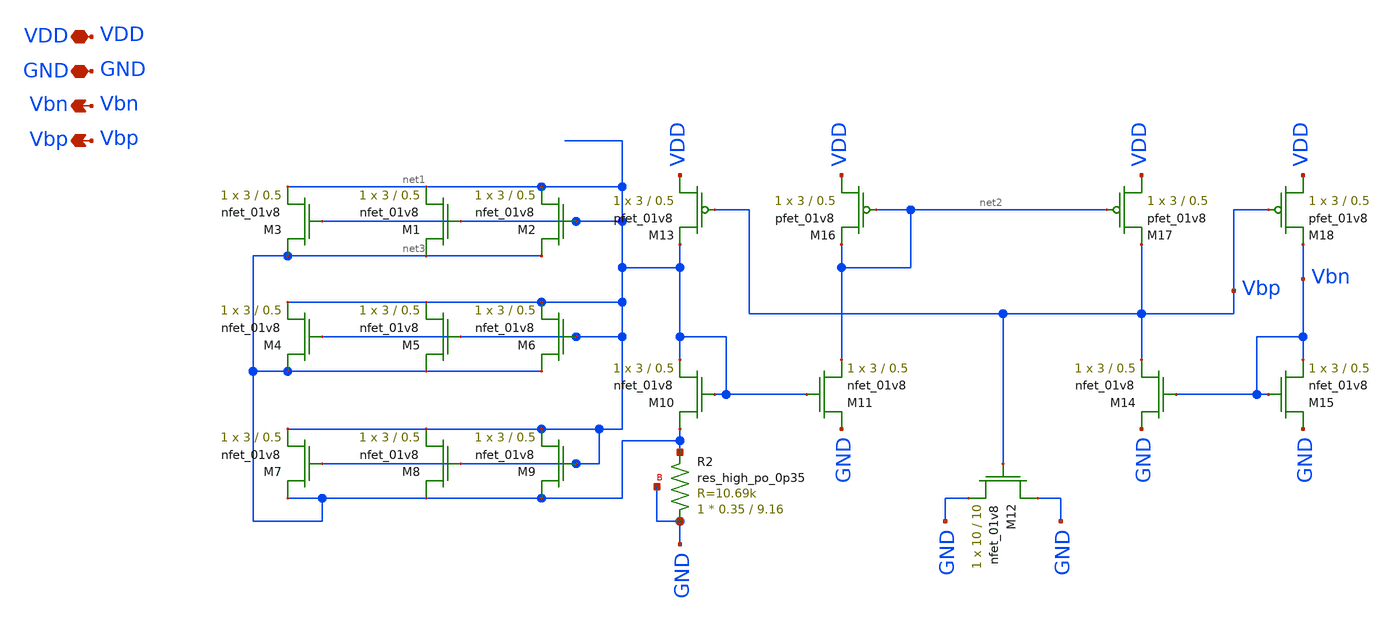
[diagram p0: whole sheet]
** sch_path: final/LDS/bias_gen_LDS.sch
**.subckt bias_gen_LDS VDD Vbp GND Vbn
*.iopin VDD
*.opin Vbp
*.iopin GND
*.opin Vbn
XM12 GND Vbp GND GND sky130_fd_pr__nfet_01v8 L=10 W=10 nf=1 ad='int((nf+1)/2) * W/nf * 0.29' as='int((nf+2)/2) * W/nf * 0.29'
+ pd='2*int((nf+1)/2) * (W/nf + 0.29)' ps='2*int((nf+2)/2) * (W/nf + 0.29)' nrd='0.29 / W' nrs='0.29 / W'
+ sa=0 sb=0 sd=0 mult=1 m=1
XM13 VDD Vbp net1 VDD sky130_fd_pr__pfet_01v8 L=0.5 W=3 nf=1 ad='int((nf+1)/2) * W/nf * 0.29' as='int((nf+2)/2) * W/nf * 0.29'
+ pd='2*int((nf+1)/2) * (W/nf + 0.29)' ps='2*int((nf+2)/2) * (W/nf + 0.29)' nrd='0.29 / W' nrs='0.29 / W'
+ sa=0 sb=0 sd=0 mult=1 m=1
XR2 GND net3 GND sky130_fd_pr__res_high_po_0p35 L=9.16 mult=1 m=1
XM3 net3 net1 net1 GND sky130_fd_pr__nfet_01v8 L=0.5 W=3 nf=1 ad='int((nf+1)/2) * W/nf * 0.29' as='int((nf+2)/2) * W/nf * 0.29'
+ pd='2*int((nf+1)/2) * (W/nf + 0.29)' ps='2*int((nf+2)/2) * (W/nf + 0.29)' nrd='0.29 / W' nrs='0.29 / W'
+ sa=0 sb=0 sd=0 mult=1 m=1
XM1 net3 net1 net1 GND sky130_fd_pr__nfet_01v8 L=0.5 W=3 nf=1 ad='int((nf+1)/2) * W/nf * 0.29' as='int((nf+2)/2) * W/nf * 0.29'
+ pd='2*int((nf+1)/2) * (W/nf + 0.29)' ps='2*int((nf+2)/2) * (W/nf + 0.29)' nrd='0.29 / W' nrs='0.29 / W'
+ sa=0 sb=0 sd=0 mult=1 m=1
XM2 net3 net1 net1 GND sky130_fd_pr__nfet_01v8 L=0.5 W=3 nf=1 ad='int((nf+1)/2) * W/nf * 0.29' as='int((nf+2)/2) * W/nf * 0.29'
+ pd='2*int((nf+1)/2) * (W/nf + 0.29)' ps='2*int((nf+2)/2) * (W/nf + 0.29)' nrd='0.29 / W' nrs='0.29 / W'
+ sa=0 sb=0 sd=0 mult=1 m=1
XM4 net3 net1 net1 GND sky130_fd_pr__nfet_01v8 L=0.5 W=3 nf=1 ad='int((nf+1)/2) * W/nf * 0.29' as='int((nf+2)/2) * W/nf * 0.29'
+ pd='2*int((nf+1)/2) * (W/nf + 0.29)' ps='2*int((nf+2)/2) * (W/nf + 0.29)' nrd='0.29 / W' nrs='0.29 / W'
+ sa=0 sb=0 sd=0 mult=1 m=1
XM5 net3 net1 net1 GND sky130_fd_pr__nfet_01v8 L=0.5 W=3 nf=1 ad='int((nf+1)/2) * W/nf * 0.29' as='int((nf+2)/2) * W/nf * 0.29'
+ pd='2*int((nf+1)/2) * (W/nf + 0.29)' ps='2*int((nf+2)/2) * (W/nf + 0.29)' nrd='0.29 / W' nrs='0.29 / W'
+ sa=0 sb=0 sd=0 mult=1 m=1
XM6 net3 net1 net1 GND sky130_fd_pr__nfet_01v8 L=0.5 W=3 nf=1 ad='int((nf+1)/2) * W/nf * 0.29' as='int((nf+2)/2) * W/nf * 0.29'
+ pd='2*int((nf+1)/2) * (W/nf + 0.29)' ps='2*int((nf+2)/2) * (W/nf + 0.29)' nrd='0.29 / W' nrs='0.29 / W'
+ sa=0 sb=0 sd=0 mult=1 m=1
XM7 net3 net1 net1 GND sky130_fd_pr__nfet_01v8 L=0.5 W=3 nf=1 ad='int((nf+1)/2) * W/nf * 0.29' as='int((nf+2)/2) * W/nf * 0.29'
+ pd='2*int((nf+1)/2) * (W/nf + 0.29)' ps='2*int((nf+2)/2) * (W/nf + 0.29)' nrd='0.29 / W' nrs='0.29 / W'
+ sa=0 sb=0 sd=0 mult=1 m=1
XM8 net3 net1 net1 GND sky130_fd_pr__nfet_01v8 L=0.5 W=3 nf=1 ad='int((nf+1)/2) * W/nf * 0.29' as='int((nf+2)/2) * W/nf * 0.29'
+ pd='2*int((nf+1)/2) * (W/nf + 0.29)' ps='2*int((nf+2)/2) * (W/nf + 0.29)' nrd='0.29 / W' nrs='0.29 / W'
+ sa=0 sb=0 sd=0 mult=1 m=1
XM9 net3 net1 net1 GND sky130_fd_pr__nfet_01v8 L=0.5 W=3 nf=1 ad='int((nf+1)/2) * W/nf * 0.29' as='int((nf+2)/2) * W/nf * 0.29'
+ pd='2*int((nf+1)/2) * (W/nf + 0.29)' ps='2*int((nf+2)/2) * (W/nf + 0.29)' nrd='0.29 / W' nrs='0.29 / W'
+ sa=0 sb=0 sd=0 mult=1 m=1
XM10 net3 net1 net1 GND sky130_fd_pr__nfet_01v8 L=0.5 W=3 nf=1 ad='int((nf+1)/2) * W/nf * 0.29' as='int((nf+2)/2) * W/nf * 0.29'
+ pd='2*int((nf+1)/2) * (W/nf + 0.29)' ps='2*int((nf+2)/2) * (W/nf + 0.29)' nrd='0.29 / W' nrs='0.29 / W'
+ sa=0 sb=0 sd=0 mult=1 m=1
XM11 GND net1 net2 GND sky130_fd_pr__nfet_01v8 L=0.5 W=3 nf=1 ad='int((nf+1)/2) * W/nf * 0.29' as='int((nf+2)/2) * W/nf * 0.29'
+ pd='2*int((nf+1)/2) * (W/nf + 0.29)' ps='2*int((nf+2)/2) * (W/nf + 0.29)' nrd='0.29 / W' nrs='0.29 / W'
+ sa=0 sb=0 sd=0 mult=1 m=1
XM14 GND Vbn Vbp GND sky130_fd_pr__nfet_01v8 L=0.5 W=3 nf=1 ad='int((nf+1)/2) * W/nf * 0.29' as='int((nf+2)/2) * W/nf * 0.29'
+ pd='2*int((nf+1)/2) * (W/nf + 0.29)' ps='2*int((nf+2)/2) * (W/nf + 0.29)' nrd='0.29 / W' nrs='0.29 / W'
+ sa=0 sb=0 sd=0 mult=1 m=1
XM15 GND Vbn Vbn GND sky130_fd_pr__nfet_01v8 L=0.5 W=3 nf=1 ad='int((nf+1)/2) * W/nf * 0.29' as='int((nf+2)/2) * W/nf * 0.29'
+ pd='2*int((nf+1)/2) * (W/nf + 0.29)' ps='2*int((nf+2)/2) * (W/nf + 0.29)' nrd='0.29 / W' nrs='0.29 / W'
+ sa=0 sb=0 sd=0 mult=1 m=1
XM16 VDD net2 net2 VDD sky130_fd_pr__pfet_01v8 L=0.5 W=3 nf=1 ad='int((nf+1)/2) * W/nf * 0.29' as='int((nf+2)/2) * W/nf * 0.29'
+ pd='2*int((nf+1)/2) * (W/nf + 0.29)' ps='2*int((nf+2)/2) * (W/nf + 0.29)' nrd='0.29 / W' nrs='0.29 / W'
+ sa=0 sb=0 sd=0 mult=1 m=1
XM17 VDD net2 Vbp VDD sky130_fd_pr__pfet_01v8 L=0.5 W=3 nf=1 ad='int((nf+1)/2) * W/nf * 0.29' as='int((nf+2)/2) * W/nf * 0.29'
+ pd='2*int((nf+1)/2) * (W/nf + 0.29)' ps='2*int((nf+2)/2) * (W/nf + 0.29)' nrd='0.29 / W' nrs='0.29 / W'
+ sa=0 sb=0 sd=0 mult=1 m=1
XM18 VDD Vbp Vbn VDD sky130_fd_pr__pfet_01v8 L=0.5 W=3 nf=1 ad='int((nf+1)/2) * W/nf * 0.29' as='int((nf+2)/2) * W/nf * 0.29'
+ pd='2*int((nf+1)/2) * (W/nf + 0.29)' ps='2*int((nf+2)/2) * (W/nf + 0.29)' nrd='0.29 / W' nrs='0.29 / W'
+ sa=0 sb=0 sd=0 mult=1 m=1
**.ends
.end
